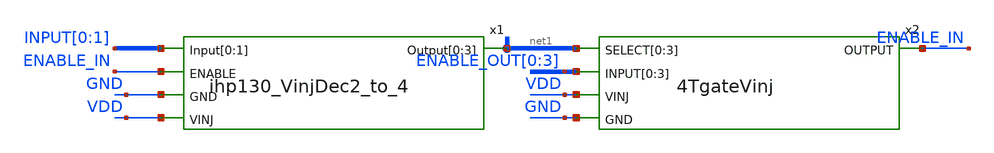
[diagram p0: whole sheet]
** sch_path: ihp130_cells/MUX/MUX.sch
**.subckt MUX
x1 INPUT[0] INPUT[1] ENABLE_IN net1[3] net1[2] net1[1] net1[0] GND VDD ihp130_VinjDec2_to_4
x2 net1[3] net1[2] net1[1] net1[0] ENABLE_IN ENABLE_OUT[0] ENABLE_OUT[1] ENABLE_OUT[2] ENABLE_OUT[3]
+ VDD GND 4TgateVinj
**.ends

* expanding   symbol:  VinjDec2_to_4/ihp130_VinjDec2_to_4.sym # of pins=5
** sym_path: ihp130_cells/VinjDec2_to_4/ihp130_VinjDec2_to_4.sym
** sch_path: ihp130_cells/VinjDec2_to_4/ihp130_VinjDec2_to_4.sch
.subckt ihp130_VinjDec2_to_4 Input[0] Input[1] ENABLE Output[0] Output[1] Output[2] Output[3] GND
+ VINJ
*.ipin VINJ
*.opin Output[0],Output[1],Output[2],Output[3]
*.ipin Input[0],Input[1]
*.ipin GND
*.ipin ENABLE
x2 VINJ Input[0] net1 GND ihp130_VinjInv2
x6 VINJ Input[1] net2 GND ihp130_VinjInv2
x7 VINJ ENABLE ENABLE_B GND ihp130_VinjInv2
x1 VINJ Input[0] Input[1] Output[0] ENABLE_B GND ihp130_VinjNOR3
x3 VINJ Input[0] net2 Output[1] ENABLE_B GND ihp130_VinjNOR3
x4 VINJ net1 Input[1] Output[2] ENABLE_B GND ihp130_VinjNOR3
x5 VINJ net1 net2 Output[3] ENABLE_B GND ihp130_VinjNOR3
.ends


* expanding   symbol:  4TgateVinj/4TgateVinj.sym # of pins=5
** sym_path: ihp130_cells/4TgateVinj/4TgateVinj.sym
** sch_path: ihp130_cells/4TgateVinj/4TgateVinj.sch
.subckt 4TgateVinj SELECT[0] SELECT[1] SELECT[2] SELECT[3] OUTPUT INPUT[0] INPUT[1] INPUT[2]
+ INPUT[3] VINJ GND
*.ipin SELECT[0],SELECT[1],SELECT[2],SELECT[3]
*.ipin INPUT[0],INPUT[1],INPUT[2],INPUT[3]
*.ipin VINJ
*.ipin GND
*.opin OUTPUT
x1 SELECT[0] INPUT[0] VINJ GND OUTPUT ihp130_TgateVinj02
x2 SELECT[1] INPUT[1] VINJ GND OUTPUT ihp130_TgateVinj02
x3 SELECT[2] INPUT[2] VINJ GND OUTPUT ihp130_TgateVinj02
x4 SELECT[3] INPUT[3] VINJ GND OUTPUT ihp130_TgateVinj02
.ends


* expanding   symbol:  VinjInv2/ihp130_VinjInv2.sym # of pins=4
** sym_path: ihp130_cells/VinjInv2/ihp130_VinjInv2.sym
** sch_path: ihp130_cells/VinjInv2/ihp130_VinjInv2.sch
.subckt ihp130_VinjInv2 VINJ Input Output GND
*.ipin VINJ
*.ipin GND
*.ipin Input
*.opin Output
XM1 Output Input GND GND sg13_hv_nmos w=0.42u l=0.53u ng=1 m=1 mm_ok=1
XM2 Output Input VINJ VINJ sg13_hv_pmos w=0.42u l=0.53u ng=1 m=1 mm_ok=1
.ends


* expanding   symbol:  VinjNOR3/ihp130_VinjNOR3.sym # of pins=6
** sym_path: ihp130_cells/VinjNOR3/ihp130_VinjNOR3.sym
** sch_path: ihp130_cells/VinjNOR3/ihp130_VinjNOR3.sch
.subckt ihp130_VinjNOR3 VINJ Input[0] Input[1] Output Input[2] GND
*.ipin Input[0]
*.ipin VINJ
*.ipin GND
*.opin Output
*.ipin Input[1]
*.ipin Input[2]
XM1 net1 Input[2] VINJ VINJ sg13_hv_pmos w=0.42u l=0.53u ng=1 m=1 mm_ok=1
XM2 net2 Input[0] net1 VINJ sg13_hv_pmos w=0.42u l=0.53u ng=1 m=1 mm_ok=1
XM3 Output Input[1] net2 VINJ sg13_hv_pmos w=0.42u l=0.53u ng=1 m=1 mm_ok=1
XM4 Output Input[1] GND GND sg13_hv_nmos w=0.42u l=0.5u ng=1 m=1 mm_ok=1
XM5 Output Input[2] GND GND sg13_hv_nmos w=0.42u l=0.5u ng=1 m=1 mm_ok=1
XM6 Output Input[0] GND GND sg13_hv_nmos w=0.42u l=0.5u ng=1 m=1 mm_ok=1
.ends


* expanding   symbol:  TgateVinj02/ihp130_TgateVinj02.sym # of pins=5
** sym_path: ihp130_cells/TgateVinj02/ihp130_TgateVinj02.sym
** sch_path: ihp130_cells/TgateVinj02/ihp130_TgateVinj02.sch
.subckt ihp130_TgateVinj02 SELECT INPUT VINJ GND OUTPUT
*.ipin SELECT
*.ipin INPUT
*.ipin VINJ
*.ipin GND
*.opin OUTPUT
XM1 Selb SELECT VINJ VINJ sg13_hv_pmos w=0.42u l=0.5u ng=1 m=1 mm_ok=1
XM2 Selb SELECT GND GND sg13_hv_nmos w=0.42u l=0.5u ng=1 m=1 mm_ok=1
XM3 INPUT Selb OUTPUT VINJ sg13_hv_pmos w=0.42u l=0.5u ng=1 m=1 mm_ok=1
XM4 INPUT SELECT OUTPUT GND sg13_hv_nmos w=0.42u l=0.5u ng=1 m=1 mm_ok=1
.ends

.end
